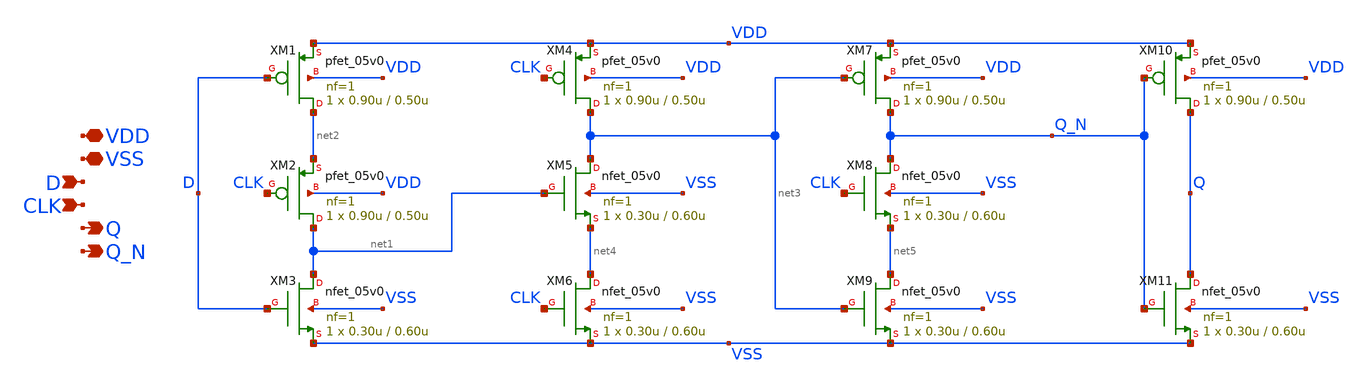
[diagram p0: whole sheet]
** sch_path: xschem/switch-matrix/dff_tspc.sch
**.subckt dff_tspc VDD VSS D CLK Q Q_N
*.iopin VDD
*.iopin VSS
*.ipin D
*.ipin CLK
*.opin Q
*.opin Q_N
XM1 net2 D VDD VDD pfet_05v0 L=0.50u W=0.90u nf=1 ad='int((nf+1)/2) * W/nf * 0.18u' as='int((nf+2)/2) * W/nf * 0.18u'
+ pd='2*int((nf+1)/2) * (W/nf + 0.18u)' ps='2*int((nf+2)/2) * (W/nf + 0.18u)' nrd='0.18u / W' nrs='0.18u / W'
+ sa=0 sb=0 sd=0 m=1
XM2 net1 CLK net2 VDD pfet_05v0 L=0.50u W=0.90u nf=1 ad='int((nf+1)/2) * W/nf * 0.18u' as='int((nf+2)/2) * W/nf * 0.18u'
+ pd='2*int((nf+1)/2) * (W/nf + 0.18u)' ps='2*int((nf+2)/2) * (W/nf + 0.18u)' nrd='0.18u / W' nrs='0.18u / W'
+ sa=0 sb=0 sd=0 m=1
XM3 net1 D VSS VSS nfet_05v0 L=0.60u W=0.30u nf=1 ad='int((nf+1)/2) * W/nf * 0.18u' as='int((nf+2)/2) * W/nf * 0.18u'
+ pd='2*int((nf+1)/2) * (W/nf + 0.18u)' ps='2*int((nf+2)/2) * (W/nf + 0.18u)' nrd='0.18u / W' nrs='0.18u / W'
+ sa=0 sb=0 sd=0 m=1
XM4 net3 CLK VDD VDD pfet_05v0 L=0.50u W=0.90u nf=1 ad='int((nf+1)/2) * W/nf * 0.18u' as='int((nf+2)/2) * W/nf * 0.18u'
+ pd='2*int((nf+1)/2) * (W/nf + 0.18u)' ps='2*int((nf+2)/2) * (W/nf + 0.18u)' nrd='0.18u / W' nrs='0.18u / W'
+ sa=0 sb=0 sd=0 m=1
XM5 net3 net1 net4 VSS nfet_05v0 L=0.60u W=0.30u nf=1 ad='int((nf+1)/2) * W/nf * 0.18u' as='int((nf+2)/2) * W/nf * 0.18u'
+ pd='2*int((nf+1)/2) * (W/nf + 0.18u)' ps='2*int((nf+2)/2) * (W/nf + 0.18u)' nrd='0.18u / W' nrs='0.18u / W'
+ sa=0 sb=0 sd=0 m=1
XM6 net4 CLK VSS VSS nfet_05v0 L=0.60u W=0.30u nf=1 ad='int((nf+1)/2) * W/nf * 0.18u' as='int((nf+2)/2) * W/nf * 0.18u'
+ pd='2*int((nf+1)/2) * (W/nf + 0.18u)' ps='2*int((nf+2)/2) * (W/nf + 0.18u)' nrd='0.18u / W' nrs='0.18u / W'
+ sa=0 sb=0 sd=0 m=1
XM7 Q_N net3 VDD VDD pfet_05v0 L=0.50u W=0.90u nf=1 ad='int((nf+1)/2) * W/nf * 0.18u' as='int((nf+2)/2) * W/nf * 0.18u'
+ pd='2*int((nf+1)/2) * (W/nf + 0.18u)' ps='2*int((nf+2)/2) * (W/nf + 0.18u)' nrd='0.18u / W' nrs='0.18u / W'
+ sa=0 sb=0 sd=0 m=1
XM8 Q_N CLK net5 VSS nfet_05v0 L=0.60u W=0.30u nf=1 ad='int((nf+1)/2) * W/nf * 0.18u' as='int((nf+2)/2) * W/nf * 0.18u'
+ pd='2*int((nf+1)/2) * (W/nf + 0.18u)' ps='2*int((nf+2)/2) * (W/nf + 0.18u)' nrd='0.18u / W' nrs='0.18u / W'
+ sa=0 sb=0 sd=0 m=1
XM9 net5 net3 VSS VSS nfet_05v0 L=0.60u W=0.30u nf=1 ad='int((nf+1)/2) * W/nf * 0.18u' as='int((nf+2)/2) * W/nf * 0.18u'
+ pd='2*int((nf+1)/2) * (W/nf + 0.18u)' ps='2*int((nf+2)/2) * (W/nf + 0.18u)' nrd='0.18u / W' nrs='0.18u / W'
+ sa=0 sb=0 sd=0 m=1
XM10 Q Q_N VDD VDD pfet_05v0 L=0.50u W=0.90u nf=1 ad='int((nf+1)/2) * W/nf * 0.18u' as='int((nf+2)/2) * W/nf * 0.18u'
+ pd='2*int((nf+1)/2) * (W/nf + 0.18u)' ps='2*int((nf+2)/2) * (W/nf + 0.18u)' nrd='0.18u / W' nrs='0.18u / W'
+ sa=0 sb=0 sd=0 m=1
XM11 Q Q_N VSS VSS nfet_05v0 L=0.60u W=0.30u nf=1 ad='int((nf+1)/2) * W/nf * 0.18u' as='int((nf+2)/2) * W/nf * 0.18u'
+ pd='2*int((nf+1)/2) * (W/nf + 0.18u)' ps='2*int((nf+2)/2) * (W/nf + 0.18u)' nrd='0.18u / W' nrs='0.18u / W'
+ sa=0 sb=0 sd=0 m=1
**.ends
.end
